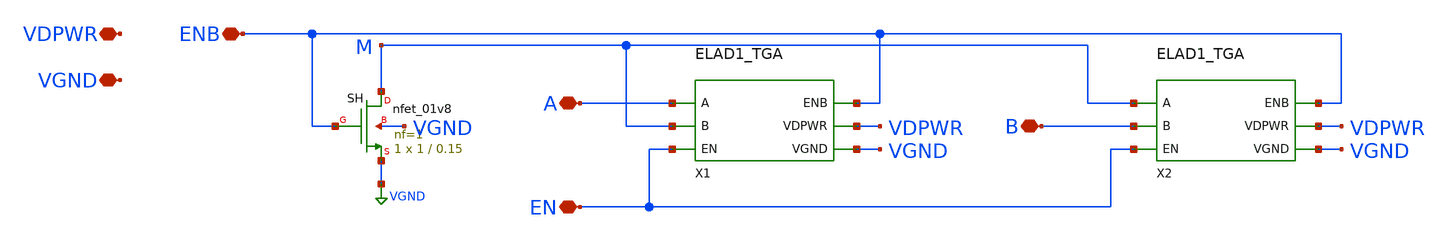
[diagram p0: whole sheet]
** sch_path: cells/ELAD1_TSW/schematic/ELAD1_TSW.sch
**.subckt ELAD1_TSW A B EN ENB VDPWR VGND
*.iopin A
*.iopin B
*.iopin EN
*.iopin ENB
*.iopin VDPWR
*.iopin VGND
X1 A M EN ENB VDPWR VGND ELAD1_TGA
X2 M B EN ENB VDPWR VGND ELAD1_TGA
XSH M ENB VGND VGND sky130_fd_pr__nfet_01v8 L=0.15 W=1 nf=1 ad='int((1 + 1)/2) * 1 / 1 * 0.29' as='int((1 + 2)/2) * 1 / 1 * 0.29'
+ pd='2*int((1 + 1)/2) * (1 / 1 + 0.29)' ps='2*int((1 + 2)/2) * (1 / 1 + 0.29)' nrd='0.29 / 1 ' nrs='0.29 / 1 '
+ sa=0 sb=0 sd=0 mult=1 m=1
**.ends

* expanding   symbol:  ELAD1_TGA.sym # of pins=6
** sym_path: cells/ELAD1_TGA/schematic/ELAD1_TGA.sym
** sch_path: cells/ELAD1_TGA/schematic/ELAD1_TGA.sch
.subckt ELAD1_TGA A B EN ENB VDPWR VGND
*.iopin A
*.iopin B
*.iopin EN
*.iopin ENB
*.iopin VDPWR
*.iopin VGND
XMN A EN B VGND sky130_fd_pr__nfet_01v8_lvt L=0.15 W=4 nf=1 ad='int((1 + 1)/2) * 4 / 1 * 0.29' as='int((1 + 2)/2) * 4 / 1 * 0.29'
+ pd='2*int((1 + 1)/2) * (4 / 1 + 0.29)' ps='2*int((1 + 2)/2) * (4 / 1 + 0.29)' nrd='0.29 / 4 ' nrs='0.29 / 4 '
+ sa=0 sb=0 sd=0 mult=1 m=1
XMP A ENB B VDPWR sky130_fd_pr__pfet_01v8_lvt L=0.35 W=12 nf=1 ad='int((1 + 1)/2) * 12 / 1 * 0.29' as='int((1 + 2)/2) * 12 / 1 * 0.29'
+ pd='2*int((1 + 1)/2) * (12 / 1 + 0.29)' ps='2*int((1 + 2)/2) * (12 / 1 + 0.29)' nrd='0.29 / 12 ' nrs='0.29 / 12 '
+ sa=0 sb=0 sd=0 mult=1 m=1
.ends

.GLOBAL VGND
.end
